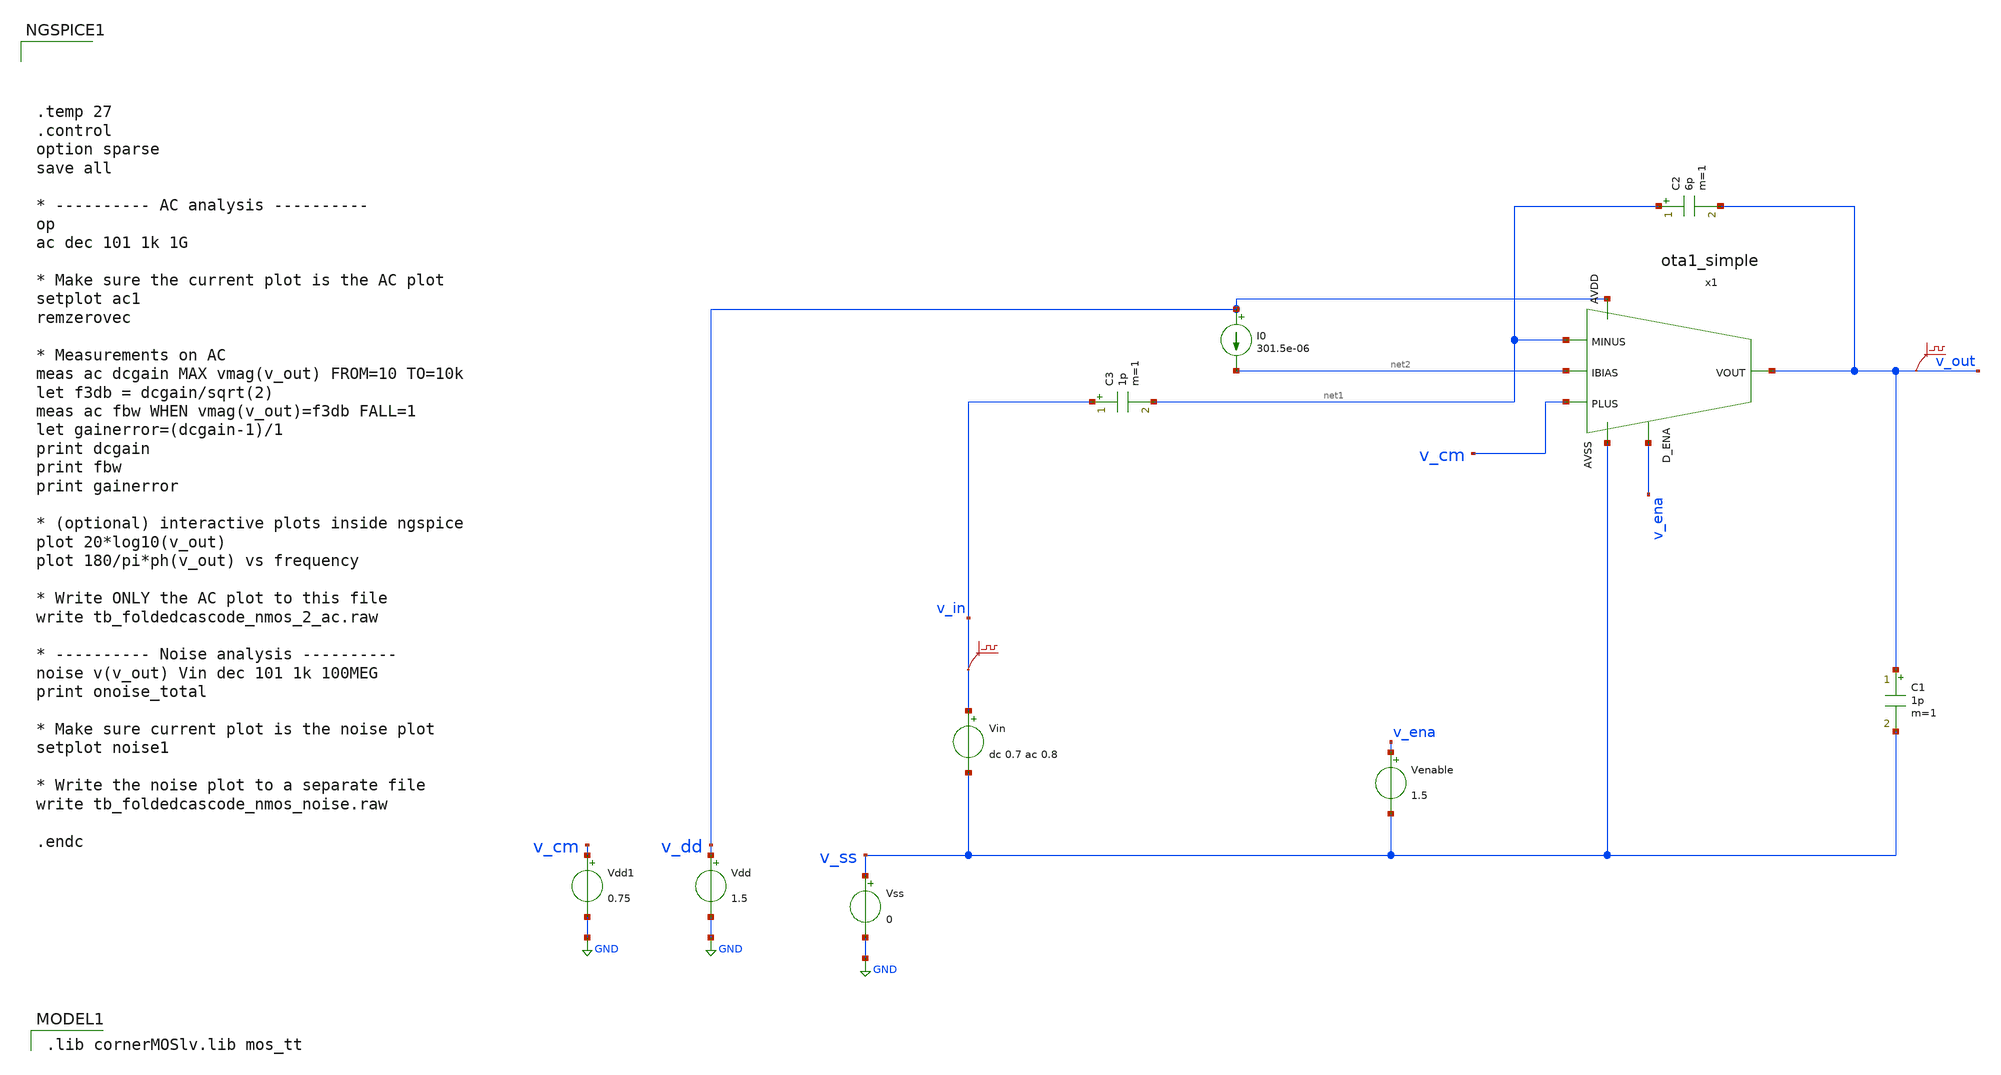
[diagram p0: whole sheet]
** sch_path: DSM_2ndOrder/1_Schematics/real_circuits/tb_otasimple_ac.sch
* (c) 2025 Thesis_HP, Apache-2.0 license
**.subckt tb_otasimple_ac
Vss v_ss GND 0
Vdd v_dd GND 1.5
Vin v_in v_ss dc 0.7 ac 0.8
.save v(v_in)
I0 v_dd net2 301.5e-06
C1 v_out v_ss 1p m=1
.save v(v_out)
Venable v_ena v_ss 1.5
x1 v_dd v_cm net1 v_out net2 v_ena v_ss ota1_simple
C2 net1 v_out 6p m=1
C3 v_in net1 1p m=1
Vdd1 v_cm GND 0.75
**** begin user architecture code
 .lib cornerMOSlv.lib mos_tt





.temp 27
.control
option sparse
save all

* ---------- AC analysis ----------
op
ac dec 101 1k 1G

* Make sure the current plot is the AC plot
setplot ac1
remzerovec

* Measurements on AC
meas ac dcgain MAX vmag(v_out) FROM=10 TO=10k
let f3db = dcgain/sqrt(2)
meas ac fbw WHEN vmag(v_out)=f3db FALL=1
let gainerror=(dcgain-1)/1
print dcgain
print fbw
print gainerror

* (optional) interactive plots inside ngspice
plot 20*log10(v_out)
plot 180/pi*ph(v_out) vs frequency

* Write ONLY the AC plot to this file
write tb_foldedcascode_nmos_2_ac.raw

* ---------- Noise analysis ----------
noise v(v_out) Vin dec 101 1k 100MEG
print onoise_total

* Make sure current plot is the noise plot
setplot noise1

* Write the noise plot to a separate file
write tb_foldedcascode_nmos_noise.raw

.endc


**** end user architecture code
**.ends

* expanding   symbol:  ota1_simple.sym # of pins=7
** sym_path: DSM_2ndOrder/1_Schematics/real_circuits/3v3/ota1_simple.sym
** sch_path: DSM_2ndOrder/1_Schematics/real_circuits/3v3/ota1_simple.sch
.subckt ota1_simple AVDD PLUS MINUS VOUT IBIAS D_ENA AVSS
*.opin VOUT
*.ipin MINUS
*.ipin PLUS
*.ipin AVSS
*.ipin IBIAS
*.ipin AVDD
*.ipin D_ENA
XM01 net9 PLUS net1 AVSS sg13_lv_nmos w=161.5u l=2u ng=17 m=1 mm_ok=1
XM02 net10 MINUS net1 AVSS sg13_lv_nmos w=161.5u l=2u ng=17 m=1 mm_ok=1
XMt net1 net6 AVSS AVSS sg13_lv_nmos w=38u l=1u ng=4 m=1 mm_ok=1
XM08 VOUT net2 net5 AVSS sg13_lv_nmos w=95u l=1.5u ng=10 m=1 mm_ok=1
XM07 net3 net2 net4 AVSS sg13_lv_nmos w=95u l=1.5u ng=10 m=1 mm_ok=1
XM03 net4 net3 AVSS AVSS sg13_lv_nmos w=95u l=1.5u ng=10 m=1 mm_ok=1
XM04 net5 net3 AVSS AVSS sg13_lv_nmos w=95u l=1.5u ng=10 m=1 mm_ok=1
XMb1 net11 net6 AVSS AVSS sg13_lv_nmos w=38u l=1u ng=4 m=1 mm_ok=1
XM05 net3 net7 net9 AVDD sg13_lv_pmos w=385u l=1.5u ng=39 m=1 mm_ok=1
XM06 VOUT net7 net10 AVDD sg13_lv_pmos w=385u l=1.5u ng=39 m=1 mm_ok=1
XM09 net9 net8 AVDD AVDD sg13_lv_pmos w=500u l=1.5u ng=50 m=1 mm_ok=1
XM10 net10 net8 AVDD AVDD sg13_lv_pmos w=500u l=1.5u ng=50 m=1 mm_ok=1
XMb IBIAS net6 AVSS AVSS sg13_lv_nmos w=38u l=1u ng=4 m=1 mm_ok=1
XMb2 net11 net3 net8 AVDD sg13_lv_pmos w=385u l=1.5u ng=39 m=1 mm_ok=1
XMb3 net8 net8 AVDD AVDD sg13_lv_pmos w=385u l=1.5u ng=39 m=1 mm_ok=1
XMb5 net7 net8 AVDD AVDD sg13_lv_pmos w=385u l=1.5u ng=39 m=1 mm_ok=1
XMb4 AVSS net3 net7 AVDD sg13_lv_pmos w=50u l=0.5u ng=5 m=1 mm_ok=1
XMb10 AVDD VOUT net2 AVSS sg13_lv_nmos w=0.15u l=0.13u ng=1 m=1 mm_ok=1
XMb9 net2 net12 AVSS AVSS sg13_lv_nmos w=0.15u l=0.13u ng=1 m=1 mm_ok=1
XMb7 net8 VOUT net12 AVSS sg13_lv_nmos w=95u l=1.5u ng=10 m=1 mm_ok=1
XMb8 net12 net12 AVSS AVSS sg13_lv_nmos w=95u l=1.5u ng=10 m=1 mm_ok=1
XMb6 net8 net8 AVDD AVDD sg13_lv_pmos w=500u l=1.5u ng=50 m=1 mm_ok=1
XMe5 IBIAS net14 net6 AVSS sg13_lv_nmos w=1u l=0.13u ng=1 m=1 mm_ok=1
XMe2 net13 D_ENA AVSS AVSS sg13_lv_nmos w=1u l=0.13u ng=1 m=1 mm_ok=1
XMe4 net14 net13 AVSS AVSS sg13_lv_nmos w=1u l=0.13u ng=1 m=1 mm_ok=1
XMe6 net3 net13 AVSS AVSS sg13_lv_nmos w=1u l=0.13u ng=1 m=1 mm_ok=1
XMe3 net14 net13 AVDD AVDD sg13_lv_pmos w=1u l=0.13u ng=1 m=1 mm_ok=1
XMe1 net13 D_ENA AVDD AVDD sg13_lv_pmos w=1u l=0.13u ng=1 m=1 mm_ok=1
.ends

.GLOBAL GND
.end
